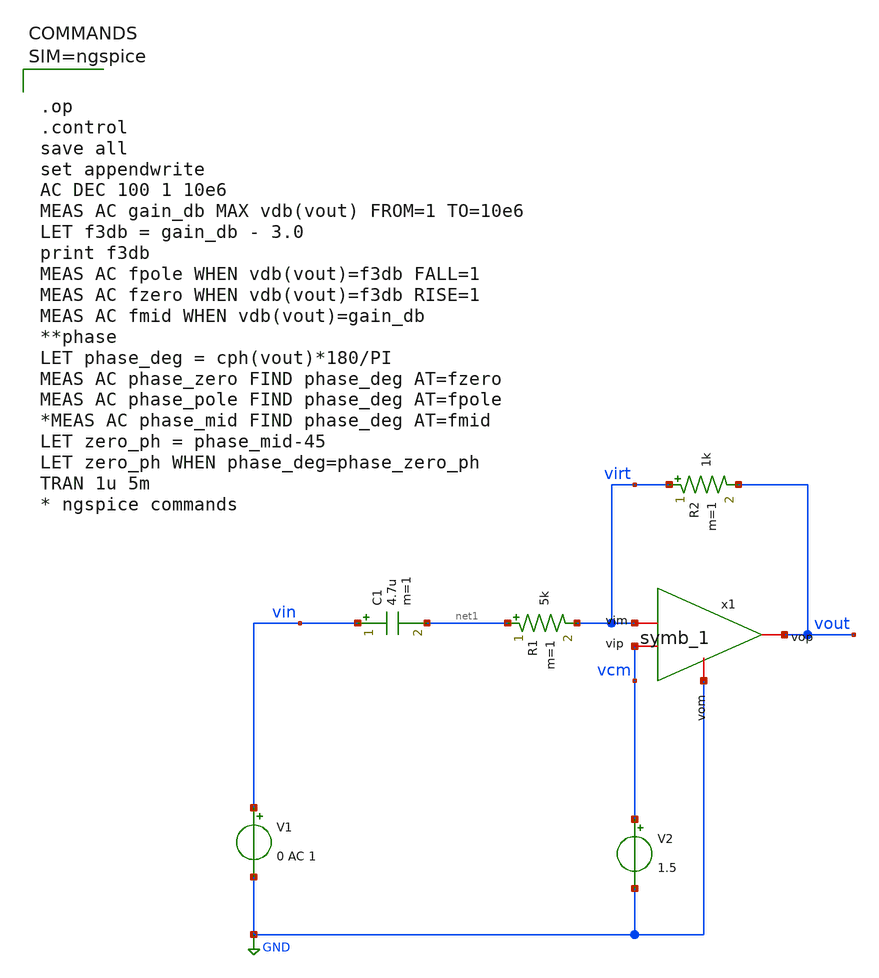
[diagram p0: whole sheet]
** sch_path: xschem/New_opam.sch
**.subckt New_opam
x1 vout vcm virt GND symb_1
R1 net1 virt 5k m=1
R2 virt vout 1k m=1
C1 vin net1 4.7u m=1
V1 vin GND 0 AC 1
V2 vcm GND 1.5
**** begin user architecture code



.op
.control
save all
set appendwrite
AC DEC 100 1 10e6
MEAS AC gain_db MAX vdb(vout) FROM=1 TO=10e6
LET f3db = gain_db - 3.0
print f3db
MEAS AC fpole WHEN vdb(vout)=f3db FALL=1
MEAS AC fzero WHEN vdb(vout)=f3db RISE=1
MEAS AC fmid WHEN vdb(vout)=gain_db
**phase
LET phase_deg = cph(vout)*180/PI
MEAS AC phase_zero FIND phase_deg AT=fzero
MEAS AC phase_pole FIND phase_deg AT=fpole
*MEAS AC phase_mid FIND phase_deg AT=fmid
LET zero_ph = phase_mid-45
LET zero_ph WHEN phase_deg=phase_zero_ph
TRAN 1u 5m
* ngspice commands



**** end user architecture code
**.ends

* expanding   symbol:  symb_1.sym # of pins=4
** sym_path: xschem/symb_1.sym
** sch_path: xschem/symb_1.sch
.subckt symb_1 vop vip vim vom
*.iopin vip
*.iopin vim
*.iopin vop
*.iopin vom
E1 vop vom vip vim 3
.ends

.GLOBAL GND
.end
